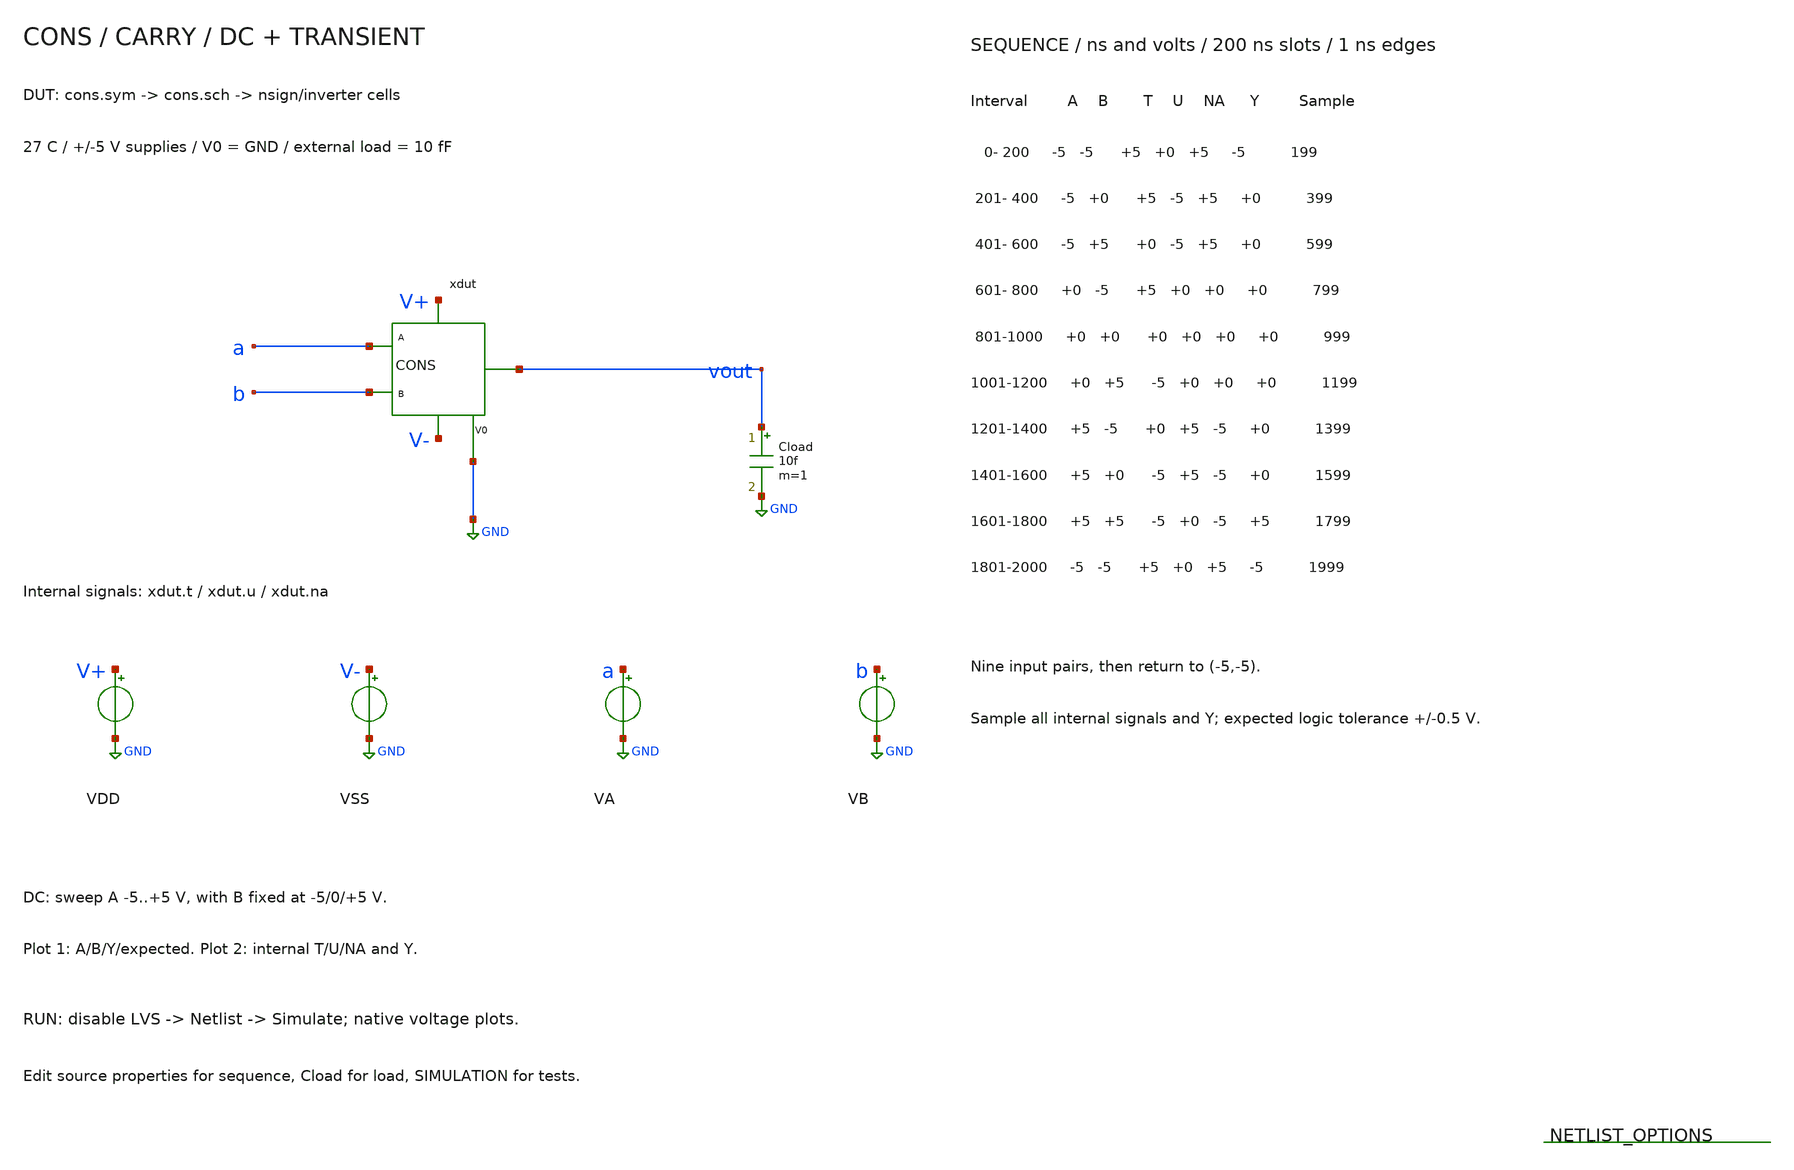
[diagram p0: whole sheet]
** sch_path: member_project/balanced-ternary-logic/PenguinEino/cons_tb.sch
**.subckt cons_tb
xdut a b vout V+ V- GND cons
Cload vout GND 10f m=1
VDD V+ GND 5
VSS V- GND -5
VA a GND PWL(0 -5 200n -5 201n -5 400n -5 401n -5 600n -5 601n 0 800n 0 801n 0 1000n 0 1001n 0 1200n
+ 0 1201n 5 1400n 5 1401n 5 1600n 5 1601n 5 1800n 5 1801n -5 2000n -5)
VB b GND PWL(0 -5 200n -5 201n 0 400n 0 401n 5 600n 5 601n -5 800n -5 801n 0 1000n 0 1001n 5 1200n 5
+ 1201n -5 1400n -5 1401n 0 1600n 0 1601n 5 1800n 5 1801n -5 2000n -5)
**** begin user architecture code
 .include $::LIB/ip62_models

.temp 27
.options rshunt=1e12
.nodeset v(xdut.t)=5 v(xdut.u)=0 v(xdut.na)=5 v(vout)=-5
.nodeset v(xdut.x_t.net1)=5 v(xdut.x_t.net2)=5 v(xdut.x_t.net3)=-5 v(xdut.x_t.net4)=-5
+ v(xdut.x_t.net5)=0 v(xdut.x_t.net6)=0
.nodeset v(xdut.x_u.net1)=5 v(xdut.x_u.net2)=5 v(xdut.x_u.net3)=-5 v(xdut.x_u.net4)=-5
+ v(xdut.x_u.net5)=0 v(xdut.x_u.net6)=0
.nodeset v(xdut.x_y.net1)=5 v(xdut.x_y.net2)=5 v(xdut.x_y.net3)=-5 v(xdut.x_y.net4)=-5
+ v(xdut.x_y.net5)=0 v(xdut.x_y.net6)=0
.nodeset v(xdut.x_na.net1)=5 v(xdut.x_na.net2)=-5
.control
save all
set wr_singlescale
set wr_vecnames
setplot const
let failures=0
reset
alter VB -5
dc VA -5 5 0.125
meas dc dc_0_0_xdut_t find v(xdut.t) at=-5
if abs(dc_0_0_xdut_t-(5)) > 0.5
let const.failures=const.failures+1
echo FAIL: dc_0_0_xdut_t expected 5 V
end
meas dc dc_0_0_xdut_u find v(xdut.u) at=-5
if abs(dc_0_0_xdut_u-(0)) > 0.5
let const.failures=const.failures+1
echo FAIL: dc_0_0_xdut_u expected 0 V
end
meas dc dc_0_0_xdut_na find v(xdut.na) at=-5
if abs(dc_0_0_xdut_na-(5)) > 0.5
let const.failures=const.failures+1
echo FAIL: dc_0_0_xdut_na expected 5 V
end
meas dc dc_0_0_vout find v(vout) at=-5
if abs(dc_0_0_vout-(-5)) > 0.5
let const.failures=const.failures+1
echo FAIL: dc_0_0_vout expected -5 V
end
meas dc dc_0_1_xdut_t find v(xdut.t) at=0
if abs(dc_0_1_xdut_t-(5)) > 0.5
let const.failures=const.failures+1
echo FAIL: dc_0_1_xdut_t expected 5 V
end
meas dc dc_0_1_xdut_u find v(xdut.u) at=0
if abs(dc_0_1_xdut_u-(0)) > 0.5
let const.failures=const.failures+1
echo FAIL: dc_0_1_xdut_u expected 0 V
end
meas dc dc_0_1_xdut_na find v(xdut.na) at=0
if abs(dc_0_1_xdut_na-(0)) > 0.5
let const.failures=const.failures+1
echo FAIL: dc_0_1_xdut_na expected 0 V
end
meas dc dc_0_1_vout find v(vout) at=0
if abs(dc_0_1_vout-(0)) > 0.5
let const.failures=const.failures+1
echo FAIL: dc_0_1_vout expected 0 V
end
meas dc dc_0_2_xdut_t find v(xdut.t) at=5
if abs(dc_0_2_xdut_t-(0)) > 0.5
let const.failures=const.failures+1
echo FAIL: dc_0_2_xdut_t expected 0 V
end
meas dc dc_0_2_xdut_u find v(xdut.u) at=5
if abs(dc_0_2_xdut_u-(5)) > 0.5
let const.failures=const.failures+1
echo FAIL: dc_0_2_xdut_u expected 5 V
end
meas dc dc_0_2_xdut_na find v(xdut.na) at=5
if abs(dc_0_2_xdut_na-(-5)) > 0.5
let const.failures=const.failures+1
echo FAIL: dc_0_2_xdut_na expected -5 V
end
meas dc dc_0_2_vout find v(vout) at=5
if abs(dc_0_2_vout-(0)) > 0.5
let const.failures=const.failures+1
echo FAIL: dc_0_2_vout expected 0 V
end
plot v(a) v(vout) ylimit -5.5 5.5 title 'CONS DC: B=-5 V'
wrdata cons_dc_b0.txt v(a) v(b) v(xdut.t) v(xdut.u) v(xdut.na) v(vout)
reset
alter VB 0
dc VA -5 5 0.125
meas dc dc_1_0_xdut_t find v(xdut.t) at=-5
if abs(dc_1_0_xdut_t-(5)) > 0.5
let const.failures=const.failures+1
echo FAIL: dc_1_0_xdut_t expected 5 V
end
meas dc dc_1_0_xdut_u find v(xdut.u) at=-5
if abs(dc_1_0_xdut_u-(-5)) > 0.5
let const.failures=const.failures+1
echo FAIL: dc_1_0_xdut_u expected -5 V
end
meas dc dc_1_0_xdut_na find v(xdut.na) at=-5
if abs(dc_1_0_xdut_na-(5)) > 0.5
let const.failures=const.failures+1
echo FAIL: dc_1_0_xdut_na expected 5 V
end
meas dc dc_1_0_vout find v(vout) at=-5
if abs(dc_1_0_vout-(0)) > 0.5
let const.failures=const.failures+1
echo FAIL: dc_1_0_vout expected 0 V
end
meas dc dc_1_1_xdut_t find v(xdut.t) at=0
if abs(dc_1_1_xdut_t-(0)) > 0.5
let const.failures=const.failures+1
echo FAIL: dc_1_1_xdut_t expected 0 V
end
meas dc dc_1_1_xdut_u find v(xdut.u) at=0
if abs(dc_1_1_xdut_u-(0)) > 0.5
let const.failures=const.failures+1
echo FAIL: dc_1_1_xdut_u expected 0 V
end
meas dc dc_1_1_xdut_na find v(xdut.na) at=0
if abs(dc_1_1_xdut_na-(0)) > 0.5
let const.failures=const.failures+1
echo FAIL: dc_1_1_xdut_na expected 0 V
end
meas dc dc_1_1_vout find v(vout) at=0
if abs(dc_1_1_vout-(0)) > 0.5
let const.failures=const.failures+1
echo FAIL: dc_1_1_vout expected 0 V
end
meas dc dc_1_2_xdut_t find v(xdut.t) at=5
if abs(dc_1_2_xdut_t-(-5)) > 0.5
let const.failures=const.failures+1
echo FAIL: dc_1_2_xdut_t expected -5 V
end
meas dc dc_1_2_xdut_u find v(xdut.u) at=5
if abs(dc_1_2_xdut_u-(5)) > 0.5
let const.failures=const.failures+1
echo FAIL: dc_1_2_xdut_u expected 5 V
end
meas dc dc_1_2_xdut_na find v(xdut.na) at=5
if abs(dc_1_2_xdut_na-(-5)) > 0.5
let const.failures=const.failures+1
echo FAIL: dc_1_2_xdut_na expected -5 V
end
meas dc dc_1_2_vout find v(vout) at=5
if abs(dc_1_2_vout-(0)) > 0.5
let const.failures=const.failures+1
echo FAIL: dc_1_2_vout expected 0 V
end
plot v(a) v(vout) ylimit -5.5 5.5 title 'CONS DC: B=0 V'
wrdata cons_dc_b1.txt v(a) v(b) v(xdut.t) v(xdut.u) v(xdut.na) v(vout)
reset
alter VB 5
dc VA -5 5 0.125
meas dc dc_2_0_xdut_t find v(xdut.t) at=-5
if abs(dc_2_0_xdut_t-(0)) > 0.5
let const.failures=const.failures+1
echo FAIL: dc_2_0_xdut_t expected 0 V
end
meas dc dc_2_0_xdut_u find v(xdut.u) at=-5
if abs(dc_2_0_xdut_u-(-5)) > 0.5
let const.failures=const.failures+1
echo FAIL: dc_2_0_xdut_u expected -5 V
end
meas dc dc_2_0_xdut_na find v(xdut.na) at=-5
if abs(dc_2_0_xdut_na-(5)) > 0.5
let const.failures=const.failures+1
echo FAIL: dc_2_0_xdut_na expected 5 V
end
meas dc dc_2_0_vout find v(vout) at=-5
if abs(dc_2_0_vout-(0)) > 0.5
let const.failures=const.failures+1
echo FAIL: dc_2_0_vout expected 0 V
end
meas dc dc_2_1_xdut_t find v(xdut.t) at=0
if abs(dc_2_1_xdut_t-(-5)) > 0.5
let const.failures=const.failures+1
echo FAIL: dc_2_1_xdut_t expected -5 V
end
meas dc dc_2_1_xdut_u find v(xdut.u) at=0
if abs(dc_2_1_xdut_u-(0)) > 0.5
let const.failures=const.failures+1
echo FAIL: dc_2_1_xdut_u expected 0 V
end
meas dc dc_2_1_xdut_na find v(xdut.na) at=0
if abs(dc_2_1_xdut_na-(0)) > 0.5
let const.failures=const.failures+1
echo FAIL: dc_2_1_xdut_na expected 0 V
end
meas dc dc_2_1_vout find v(vout) at=0
if abs(dc_2_1_vout-(0)) > 0.5
let const.failures=const.failures+1
echo FAIL: dc_2_1_vout expected 0 V
end
meas dc dc_2_2_xdut_t find v(xdut.t) at=5
if abs(dc_2_2_xdut_t-(-5)) > 0.5
let const.failures=const.failures+1
echo FAIL: dc_2_2_xdut_t expected -5 V
end
meas dc dc_2_2_xdut_u find v(xdut.u) at=5
if abs(dc_2_2_xdut_u-(0)) > 0.5
let const.failures=const.failures+1
echo FAIL: dc_2_2_xdut_u expected 0 V
end
meas dc dc_2_2_xdut_na find v(xdut.na) at=5
if abs(dc_2_2_xdut_na-(-5)) > 0.5
let const.failures=const.failures+1
echo FAIL: dc_2_2_xdut_na expected -5 V
end
meas dc dc_2_2_vout find v(vout) at=5
if abs(dc_2_2_vout-(5)) > 0.5
let const.failures=const.failures+1
echo FAIL: dc_2_2_vout expected 5 V
end
plot v(a) v(vout) ylimit -5.5 5.5 title 'CONS DC: B=5 V'
wrdata cons_dc_b2.txt v(a) v(b) v(xdut.t) v(xdut.u) v(xdut.na) v(vout)
reset
tran 0.2n 2000n
let expected=5*((v(a)>2.5)*(v(b)>2.5)-(v(a)<-2.5)*(v(b)<-2.5))
plot v(a) v(b) v(vout) expected title 'CONS: inputs, output and expected logic'
plot v(xdut.t) v(xdut.u) v(xdut.na) v(vout) title 'CONS: internal T / U / NA / Y'
wrdata cons_tran.txt v(a) v(b) v(xdut.t) v(xdut.u) v(xdut.na) v(vout)
meas tran tran_0_xdut_t find v(xdut.t) at=199n
if abs(tran_0_xdut_t-(5)) > 0.5
let const.failures=const.failures+1
echo FAIL: tran_0_xdut_t expected 5 V
end
meas tran tran_0_xdut_u find v(xdut.u) at=199n
if abs(tran_0_xdut_u-(0)) > 0.5
let const.failures=const.failures+1
echo FAIL: tran_0_xdut_u expected 0 V
end
meas tran tran_0_xdut_na find v(xdut.na) at=199n
if abs(tran_0_xdut_na-(5)) > 0.5
let const.failures=const.failures+1
echo FAIL: tran_0_xdut_na expected 5 V
end
meas tran tran_0_vout find v(vout) at=199n
if abs(tran_0_vout-(-5)) > 0.5
let const.failures=const.failures+1
echo FAIL: tran_0_vout expected -5 V
end
meas tran tran_1_xdut_t find v(xdut.t) at=399n
if abs(tran_1_xdut_t-(5)) > 0.5
let const.failures=const.failures+1
echo FAIL: tran_1_xdut_t expected 5 V
end
meas tran tran_1_xdut_u find v(xdut.u) at=399n
if abs(tran_1_xdut_u-(-5)) > 0.5
let const.failures=const.failures+1
echo FAIL: tran_1_xdut_u expected -5 V
end
meas tran tran_1_xdut_na find v(xdut.na) at=399n
if abs(tran_1_xdut_na-(5)) > 0.5
let const.failures=const.failures+1
echo FAIL: tran_1_xdut_na expected 5 V
end
meas tran tran_1_vout find v(vout) at=399n
if abs(tran_1_vout-(0)) > 0.5
let const.failures=const.failures+1
echo FAIL: tran_1_vout expected 0 V
end
meas tran tran_2_xdut_t find v(xdut.t) at=599n
if abs(tran_2_xdut_t-(0)) > 0.5
let const.failures=const.failures+1
echo FAIL: tran_2_xdut_t expected 0 V
end
meas tran tran_2_xdut_u find v(xdut.u) at=599n
if abs(tran_2_xdut_u-(-5)) > 0.5
let const.failures=const.failures+1
echo FAIL: tran_2_xdut_u expected -5 V
end
meas tran tran_2_xdut_na find v(xdut.na) at=599n
if abs(tran_2_xdut_na-(5)) > 0.5
let const.failures=const.failures+1
echo FAIL: tran_2_xdut_na expected 5 V
end
meas tran tran_2_vout find v(vout) at=599n
if abs(tran_2_vout-(0)) > 0.5
let const.failures=const.failures+1
echo FAIL: tran_2_vout expected 0 V
end
meas tran tran_3_xdut_t find v(xdut.t) at=799n
if abs(tran_3_xdut_t-(5)) > 0.5
let const.failures=const.failures+1
echo FAIL: tran_3_xdut_t expected 5 V
end
meas tran tran_3_xdut_u find v(xdut.u) at=799n
if abs(tran_3_xdut_u-(0)) > 0.5
let const.failures=const.failures+1
echo FAIL: tran_3_xdut_u expected 0 V
end
meas tran tran_3_xdut_na find v(xdut.na) at=799n
if abs(tran_3_xdut_na-(0)) > 0.5
let const.failures=const.failures+1
echo FAIL: tran_3_xdut_na expected 0 V
end
meas tran tran_3_vout find v(vout) at=799n
if abs(tran_3_vout-(0)) > 0.5
let const.failures=const.failures+1
echo FAIL: tran_3_vout expected 0 V
end
meas tran tran_4_xdut_t find v(xdut.t) at=999n
if abs(tran_4_xdut_t-(0)) > 0.5
let const.failures=const.failures+1
echo FAIL: tran_4_xdut_t expected 0 V
end
meas tran tran_4_xdut_u find v(xdut.u) at=999n
if abs(tran_4_xdut_u-(0)) > 0.5
let const.failures=const.failures+1
echo FAIL: tran_4_xdut_u expected 0 V
end
meas tran tran_4_xdut_na find v(xdut.na) at=999n
if abs(tran_4_xdut_na-(0)) > 0.5
let const.failures=const.failures+1
echo FAIL: tran_4_xdut_na expected 0 V
end
meas tran tran_4_vout find v(vout) at=999n
if abs(tran_4_vout-(0)) > 0.5
let const.failures=const.failures+1
echo FAIL: tran_4_vout expected 0 V
end
meas tran tran_5_xdut_t find v(xdut.t) at=1199n
if abs(tran_5_xdut_t-(-5)) > 0.5
let const.failures=const.failures+1
echo FAIL: tran_5_xdut_t expected -5 V
end
meas tran tran_5_xdut_u find v(xdut.u) at=1199n
if abs(tran_5_xdut_u-(0)) > 0.5
let const.failures=const.failures+1
echo FAIL: tran_5_xdut_u expected 0 V
end
meas tran tran_5_xdut_na find v(xdut.na) at=1199n
if abs(tran_5_xdut_na-(0)) > 0.5
let const.failures=const.failures+1
echo FAIL: tran_5_xdut_na expected 0 V
end
meas tran tran_5_vout find v(vout) at=1199n
if abs(tran_5_vout-(0)) > 0.5
let const.failures=const.failures+1
echo FAIL: tran_5_vout expected 0 V
end
meas tran tran_6_xdut_t find v(xdut.t) at=1399n
if abs(tran_6_xdut_t-(0)) > 0.5
let const.failures=const.failures+1
echo FAIL: tran_6_xdut_t expected 0 V
end
meas tran tran_6_xdut_u find v(xdut.u) at=1399n
if abs(tran_6_xdut_u-(5)) > 0.5
let const.failures=const.failures+1
echo FAIL: tran_6_xdut_u expected 5 V
end
meas tran tran_6_xdut_na find v(xdut.na) at=1399n
if abs(tran_6_xdut_na-(-5)) > 0.5
let const.failures=const.failures+1
echo FAIL: tran_6_xdut_na expected -5 V
end
meas tran tran_6_vout find v(vout) at=1399n
if abs(tran_6_vout-(0)) > 0.5
let const.failures=const.failures+1
echo FAIL: tran_6_vout expected 0 V
end
meas tran tran_7_xdut_t find v(xdut.t) at=1599n
if abs(tran_7_xdut_t-(-5)) > 0.5
let const.failures=const.failures+1
echo FAIL: tran_7_xdut_t expected -5 V
end
meas tran tran_7_xdut_u find v(xdut.u) at=1599n
if abs(tran_7_xdut_u-(5)) > 0.5
let const.failures=const.failures+1
echo FAIL: tran_7_xdut_u expected 5 V
end
meas tran tran_7_xdut_na find v(xdut.na) at=1599n
if abs(tran_7_xdut_na-(-5)) > 0.5
let const.failures=const.failures+1
echo FAIL: tran_7_xdut_na expected -5 V
end
meas tran tran_7_vout find v(vout) at=1599n
if abs(tran_7_vout-(0)) > 0.5
let const.failures=const.failures+1
echo FAIL: tran_7_vout expected 0 V
end
meas tran tran_8_xdut_t find v(xdut.t) at=1799n
if abs(tran_8_xdut_t-(-5)) > 0.5
let const.failures=const.failures+1
echo FAIL: tran_8_xdut_t expected -5 V
end
meas tran tran_8_xdut_u find v(xdut.u) at=1799n
if abs(tran_8_xdut_u-(0)) > 0.5
let const.failures=const.failures+1
echo FAIL: tran_8_xdut_u expected 0 V
end
meas tran tran_8_xdut_na find v(xdut.na) at=1799n
if abs(tran_8_xdut_na-(-5)) > 0.5
let const.failures=const.failures+1
echo FAIL: tran_8_xdut_na expected -5 V
end
meas tran tran_8_vout find v(vout) at=1799n
if abs(tran_8_vout-(5)) > 0.5
let const.failures=const.failures+1
echo FAIL: tran_8_vout expected 5 V
end
meas tran tran_9_xdut_t find v(xdut.t) at=1999n
if abs(tran_9_xdut_t-(5)) > 0.5
let const.failures=const.failures+1
echo FAIL: tran_9_xdut_t expected 5 V
end
meas tran tran_9_xdut_u find v(xdut.u) at=1999n
if abs(tran_9_xdut_u-(0)) > 0.5
let const.failures=const.failures+1
echo FAIL: tran_9_xdut_u expected 0 V
end
meas tran tran_9_xdut_na find v(xdut.na) at=1999n
if abs(tran_9_xdut_na-(5)) > 0.5
let const.failures=const.failures+1
echo FAIL: tran_9_xdut_na expected 5 V
end
meas tran tran_9_vout find v(vout) at=1999n
if abs(tran_9_vout-(-5)) > 0.5
let const.failures=const.failures+1
echo FAIL: tran_9_vout expected -5 V
end
if const.failures = 0
echo PASS: CONS DC and transient internal/output samples
else
echo FAIL: CONS samples outside +/-0.5 V
end
print const.failures
.endc

**** end user architecture code
**.ends

* expanding   symbol:  /home/ishi-kai/balanced-ternary-logic/cons.sym # of pins=6
** sym_path: member_project/balanced-ternary-logic/PenguinEino/cons.sym
** sch_path: member_project/balanced-ternary-logic/PenguinEino/cons.sch
.subckt cons a b vout V+ V- V0
*.ipin a
*.ipin b
*.opin vout
*.iopin V+
*.iopin V-
*.iopin V0
x_t a b t V+ V- V0 nsign
x_u b t u V+ V- V0 nsign
x_na a na V+ V- inverter
x_y na u vout V+ V- V0 nsign
.ends


* expanding   symbol:  /home/ishi-kai/balanced-ternary-logic/nsign.sym # of pins=6
** sym_path: member_project/balanced-ternary-logic/PenguinEino/nsign.sym
** sch_path: member_project/balanced-ternary-logic/PenguinEino/nsign.sch
.subckt nsign a b vout V+ V- V0
*.iopin V+
*.ipin a
*.ipin b
*.opin vout
*.iopin V-
*.iopin V0
XXM3 net2 b net1 V+ PMOS w=34u l=1u nrd=0 nrs=0 m=1
XR2 net2 vout V+ F_RR w=2.8e-06 l=16e-06 R=1 tc1=0 tc2=0 m=1
XR1 vout net3 V+ F_RR w=2.8e-06 l=16e-06 R=1 tc1=0 tc2=0 m=1
XXM2 net3 a net4 V- NMOS w=11u l=1u nrd=0 nrs=0 m=1
XXM1 net4 b V- V- NMOS w=11u l=1u nrd=0 nrs=0 m=1
XXM5 net1 a V+ V+ PMOS w=34u l=1u nrd=0 nrs=0 m=1
XXM6 net5 a vout V+ PMOS w=14u l=1u nrd=0 nrs=0 m=1
XXM7 net5 b V0 V- NMOS w=8u l=1u nrd=0 nrs=0 m=1
XXM8 net6 b vout V+ PMOS w=14u l=1u nrd=0 nrs=0 m=1
XXM9 net6 a V0 V- NMOS w=8u l=1u nrd=0 nrs=0 m=1
.ends


* expanding   symbol:  /home/ishi-kai/balanced-ternary-logic/inverter.sym # of pins=4
** sym_path: member_project/balanced-ternary-logic/PenguinEino/inverter.sym
** sch_path: member_project/balanced-ternary-logic/PenguinEino/inverter.sch
.subckt inverter vin vout VDD VSS
*.iopin VDD
*.ipin vin
*.opin vout
*.iopin VSS
XXM1 net1 vin VDD VDD PMOS w=13.5u l=1u nrd=0 nrs=0 m=1
XR1 net1 vout VDD F_RR w=2.8e-06 l=30e-06 R=1 tc1=0 tc2=0 m=1
XR2 vout net2 VDD F_RR w=2.8e-06 l=30e-06 R=1 tc1=0 tc2=0 m=1
XXM2 net2 vin VSS VSS NMOS w=5u l=1u nrd=0 nrs=0 m=1
.ends

.GLOBAL GND
.end
